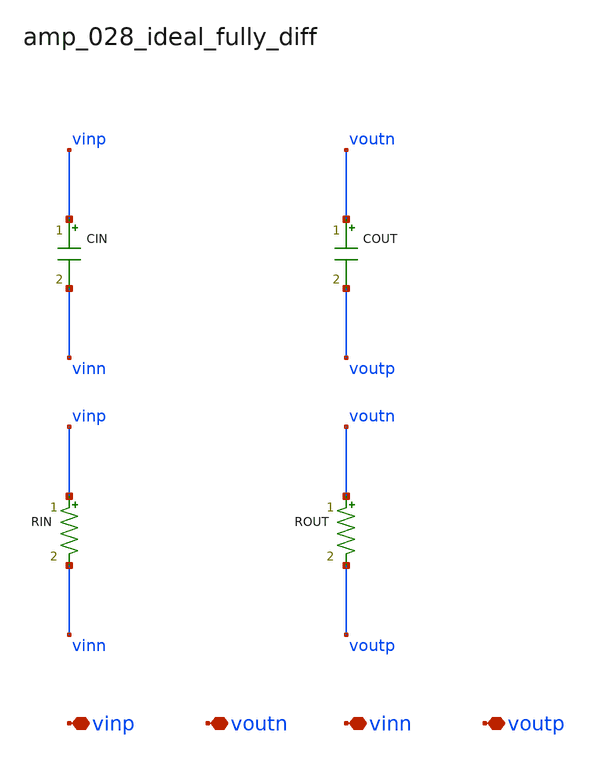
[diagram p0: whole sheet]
** sch_path: analog-db/raw/amp_028_ideal_fully_diff/amp_028_ideal_fully_diff.sch
**.subckt amp_028_ideal_fully_diff vinp voutn vinn voutp
*.iopin vinp
*.iopin voutn
*.iopin vinn
*.iopin voutp
CIN vinp vinn 'cin_val' m=1
COUT voutn voutp 'cout_val' m=1
RIN vinp vinn 'rin_val' m=1
ROUT voutn voutp 'rout_val' m=1
**.ends
.end
